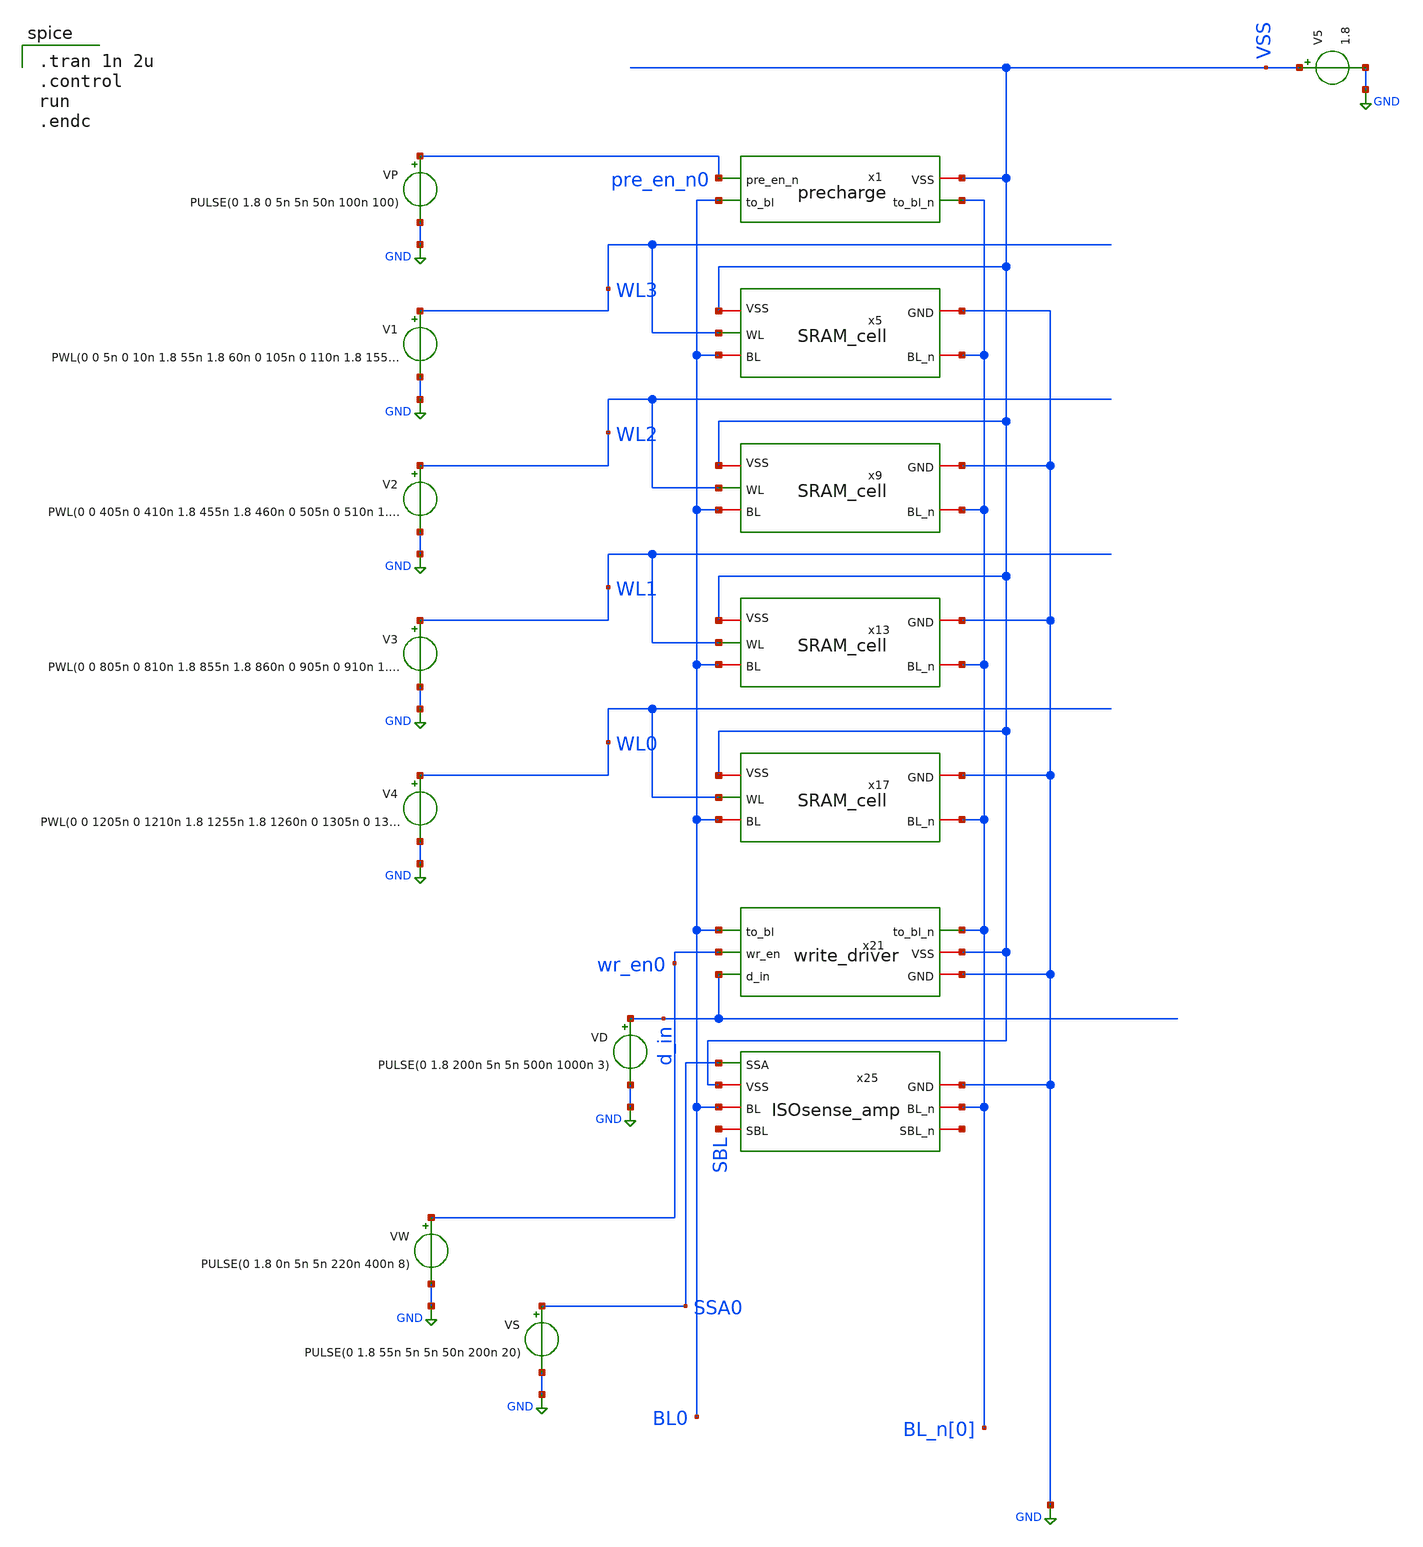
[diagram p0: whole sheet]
** sch_path: 4x1_SRAM.sch
**.subckt 4x1_SRAM
x1 VSS BL_n[0] BL0 pre_en_n0 precharge
x5 WL3 VSS BL_n[0] BL0 GND SRAM_cell
x9 WL2 VSS BL_n[0] BL0 GND SRAM_cell
x13 WL1 VSS BL_n[0] BL0 GND SRAM_cell
x17 WL0 VSS BL_n[0] BL0 GND SRAM_cell
x21 BL_n[0] BL0 wr_en0 VSS d_in GND write_driver
x25 SSA0 BL0 BL_n[0] VSS SBL net1 GND ISOsense_amp
VP pre_en_n0 GND PULSE(0 1.8 0 5n 5n 50n 100n 100)
V5 VSS GND 1.8
VW wr_en0 GND PULSE(0 1.8 0n 5n 5n 220n 400n 8)
VS SSA0 GND PULSE(0 1.8 55n 5n 5n 50n 200n 20)
V1 WL3 GND PWL(0 0 5n 0 10n 1.8 55n 1.8 60n 0 105n 0 110n 1.8 155n 1.8 160n 0 205n 0 210n 1.8 255n
+ 1.8 260n 0 305n 0 310n 1.8 355n 1.8 360n 0 1605n 0 1610n 1.8 1655n 1.8 1660n 0 2000n 0)
V2 WL2 GND PWL(0 0 405n 0 410n 1.8 455n 1.8 460n 0 505n 0 510n 1.8 555n 1.8 560n 0 605n 0 610n 1.8
+ 655n 1.8 660n 0 705n 0 710n 1.8 755n 1.8 760n 0 1705n 0 1710n 1.8 1755n 1.8 1760n 0 2000n 0)
V3 WL1 GND PWL(0 0 805n 0 810n 1.8 855n 1.8 860n 0 905n 0 910n 1.8 955n 1.8 960n 0 1005n 0 1010n 1.8
+ 1055n 1.8 1060n 0 1105n 0 1110n 1.8 1155n 1.8 1160n 0 1805n 0 1810n 1.8 1855n 1.8 1860n 0 2000n 0)
V4 WL0 GND PWL(0 0 1205n 0 1210n 1.8 1255n 1.8 1260n 0 1305n 0 1310n 1.8 1355n 1.8 1360n 0 1405n 0
+ 1410n 1.8 1455n 1.8 1460n 0 1505n 0 1510n 1.8 1555n 1.8 1560n 0 1905n 0 1910n 1.8 1955n 1.8 1960n 0 2000n
+ 0)
VD d_in GND PULSE(0 1.8 200n 5n 5n 500n 1000n 3)
**** begin user architecture code
 .lib $::SKYWATER_MODELS/sky130.lib.spice tt

.tran 1n 2u
.control
run
.endc

**** end user architecture code
**.ends

* expanding   symbol:  EE431_FINALPROJECT/proj_SRAM/precharge.sym # of pins=4
** sym_path: precharge.sym
** sch_path: precharge.sch
.subckt precharge VSS to_bl_n to_bl pre_en_n
*.ipin pre_en_n
*.opin to_bl
*.opin to_bl_n
*.iopin VSS
XM1 to_bl_n pre_en_n VSS VSS sky130_fd_pr__pfet_01v8 L=0.25 W=0.5 nf=1 ad='int((nf+1)/2) * W/nf * 0.29'
+ as='int((nf+2)/2) * W/nf * 0.29' pd='2*int((nf+1)/2) * (W/nf + 0.29)' ps='2*int((nf+2)/2) * (W/nf + 0.29)'
+ nrd='0.29 / W' nrs='0.29 / W' sa=0 sb=0 sd=0 mult=1 m=1
XM2 to_bl pre_en_n VSS VSS sky130_fd_pr__pfet_01v8 L=0.25 W=0.5 nf=1 ad='int((nf+1)/2) * W/nf * 0.29'
+ as='int((nf+2)/2) * W/nf * 0.29' pd='2*int((nf+1)/2) * (W/nf + 0.29)' ps='2*int((nf+2)/2) * (W/nf + 0.29)'
+ nrd='0.29 / W' nrs='0.29 / W' sa=0 sb=0 sd=0 mult=1 m=1
.ends


* expanding   symbol:  EE431_FINALPROJECT/proj_SRAM/SRAM_cell.sym # of pins=5
** sym_path: SRAM_cell.sym
** sch_path: SRAM_cell.sch
.subckt SRAM_cell WL VSS BL_n BL GND
*.ipin WL
*.iopin BL
*.iopin BL_n
*.iopin VSS
*.iopin GND
XM1 Q_n Q GND GND sky130_fd_pr__nfet_01v8 L=0.25 W=1.25 nf=1 ad='int((nf+1)/2) * W/nf * 0.29' as='int((nf+2)/2) * W/nf * 0.29'
+ pd='2*int((nf+1)/2) * (W/nf + 0.29)' ps='2*int((nf+2)/2) * (W/nf + 0.29)' nrd='0.29 / W' nrs='0.29 / W'
+ sa=0 sb=0 sd=0 mult=1 m=1
XM2 Q_n Q VSS VSS sky130_fd_pr__pfet_01v8 L=0.25 W=0.5 nf=1 ad='int((nf+1)/2) * W/nf * 0.29' as='int((nf+2)/2) * W/nf * 0.29'
+ pd='2*int((nf+1)/2) * (W/nf + 0.29)' ps='2*int((nf+2)/2) * (W/nf + 0.29)' nrd='0.29 / W' nrs='0.29 / W'
+ sa=0 sb=0 sd=0 mult=1 m=1
XM3 Q Q_n GND GND sky130_fd_pr__nfet_01v8 L=0.25 W=1.25 nf=1 ad='int((nf+1)/2) * W/nf * 0.29' as='int((nf+2)/2) * W/nf * 0.29'
+ pd='2*int((nf+1)/2) * (W/nf + 0.29)' ps='2*int((nf+2)/2) * (W/nf + 0.29)' nrd='0.29 / W' nrs='0.29 / W'
+ sa=0 sb=0 sd=0 mult=1 m=1
XM4 Q Q_n VSS VSS sky130_fd_pr__pfet_01v8 L=0.25 W=0.5 nf=1 ad='int((nf+1)/2) * W/nf * 0.29' as='int((nf+2)/2) * W/nf * 0.29'
+ pd='2*int((nf+1)/2) * (W/nf + 0.29)' ps='2*int((nf+2)/2) * (W/nf + 0.29)' nrd='0.29 / W' nrs='0.29 / W'
+ sa=0 sb=0 sd=0 mult=1 m=1
XM5 Q WL BL GND sky130_fd_pr__nfet_01v8 L=0.25 W=0.75 nf=1 ad='int((nf+1)/2) * W/nf * 0.29' as='int((nf+2)/2) * W/nf * 0.29'
+ pd='2*int((nf+1)/2) * (W/nf + 0.29)' ps='2*int((nf+2)/2) * (W/nf + 0.29)' nrd='0.29 / W' nrs='0.29 / W'
+ sa=0 sb=0 sd=0 mult=1 m=1
XM6 Q_n WL BL_n GND sky130_fd_pr__nfet_01v8 L=0.25 W=0.75 nf=1 ad='int((nf+1)/2) * W/nf * 0.29' as='int((nf+2)/2) * W/nf * 0.29'
+ pd='2*int((nf+1)/2) * (W/nf + 0.29)' ps='2*int((nf+2)/2) * (W/nf + 0.29)' nrd='0.29 / W' nrs='0.29 / W'
+ sa=0 sb=0 sd=0 mult=1 m=1
.ends


* expanding   symbol:  EE431_FINALPROJECT/proj_SRAM/write_driver.sym # of pins=6
** sym_path: write_driver.sym
** sch_path: write_driver.sch
.subckt write_driver to_bl_n to_bl wr_en VSS d_in GND
*.ipin d_in
*.ipin wr_en
*.opin to_bl
*.opin to_bl_n
*.iopin VSS
*.iopin GND
XM1 to_bl wr_en d_in GND sky130_fd_pr__nfet_01v8 L=0.25 W=1 nf=1 ad='int((nf+1)/2) * W/nf * 0.29' as='int((nf+2)/2) * W/nf * 0.29'
+ pd='2*int((nf+1)/2) * (W/nf + 0.29)' ps='2*int((nf+2)/2) * (W/nf + 0.29)' nrd='0.29 / W' nrs='0.29 / W'
+ sa=0 sb=0 sd=0 mult=1 m=1
XM2 to_bl_n wr_en d_n GND sky130_fd_pr__nfet_01v8 L=0.25 W=1 nf=1 ad='int((nf+1)/2) * W/nf * 0.29' as='int((nf+2)/2) * W/nf * 0.29'
+ pd='2*int((nf+1)/2) * (W/nf + 0.29)' ps='2*int((nf+2)/2) * (W/nf + 0.29)' nrd='0.29 / W' nrs='0.29 / W'
+ sa=0 sb=0 sd=0 mult=1 m=1
XM3 d_n d_in VSS VSS sky130_fd_pr__pfet_01v8 L=0.25 W=1 nf=1 ad='int((nf+1)/2) * W/nf * 0.29' as='int((nf+2)/2) * W/nf * 0.29'
+ pd='2*int((nf+1)/2) * (W/nf + 0.29)' ps='2*int((nf+2)/2) * (W/nf + 0.29)' nrd='0.29 / W' nrs='0.29 / W'
+ sa=0 sb=0 sd=0 mult=1 m=1
XM4 d_n d_in GND GND sky130_fd_pr__nfet_01v8 L=0.25 W=0.5 nf=1 ad='int((nf+1)/2) * W/nf * 0.29' as='int((nf+2)/2) * W/nf * 0.29'
+ pd='2*int((nf+1)/2) * (W/nf + 0.29)' ps='2*int((nf+2)/2) * (W/nf + 0.29)' nrd='0.29 / W' nrs='0.29 / W'
+ sa=0 sb=0 sd=0 mult=1 m=1
.ends


* expanding   symbol:  EE431_FINALPROJECT/proj_SRAM/ISOsense_amp.sym # of pins=7
** sym_path: ISOsense_amp.sym
** sch_path: ISOsense_amp.sch
.subckt ISOsense_amp SSA BL BL_n VSS SBL SBL_n GND
*.iopin VSS
*.iopin BL_n
*.iopin BL
*.iopin GND
*.ipin SSA
*.iopin SBL
*.iopin SBL_n
XM1 SBL_n SBL net1 GND sky130_fd_pr__nfet_01v8 L=0.25 W=1 nf=1 ad='int((nf+1)/2) * W/nf * 0.29' as='int((nf+2)/2) * W/nf * 0.29'
+ pd='2*int((nf+1)/2) * (W/nf + 0.29)' ps='2*int((nf+2)/2) * (W/nf + 0.29)' nrd='0.29 / W' nrs='0.29 / W'
+ sa=0 sb=0 sd=0 mult=1 m=1
XM2 SBL SBL_n net1 GND sky130_fd_pr__nfet_01v8 L=0.25 W=1 nf=1 ad='int((nf+1)/2) * W/nf * 0.29' as='int((nf+2)/2) * W/nf * 0.29'
+ pd='2*int((nf+1)/2) * (W/nf + 0.29)' ps='2*int((nf+2)/2) * (W/nf + 0.29)' nrd='0.29 / W' nrs='0.29 / W'
+ sa=0 sb=0 sd=0 mult=1 m=1
XM3 SBL_n SBL VSS VSS sky130_fd_pr__pfet_01v8 L=0.25 W=2 nf=1 ad='int((nf+1)/2) * W/nf * 0.29' as='int((nf+2)/2) * W/nf * 0.29'
+ pd='2*int((nf+1)/2) * (W/nf + 0.29)' ps='2*int((nf+2)/2) * (W/nf + 0.29)' nrd='0.29 / W' nrs='0.29 / W'
+ sa=0 sb=0 sd=0 mult=1 m=1
XM4 SBL SBL_n VSS VSS sky130_fd_pr__pfet_01v8 L=0.25 W=2 nf=1 ad='int((nf+1)/2) * W/nf * 0.29' as='int((nf+2)/2) * W/nf * 0.29'
+ pd='2*int((nf+1)/2) * (W/nf + 0.29)' ps='2*int((nf+2)/2) * (W/nf + 0.29)' nrd='0.29 / W' nrs='0.29 / W'
+ sa=0 sb=0 sd=0 mult=1 m=1
XM5 net1 SSA GND GND sky130_fd_pr__nfet_01v8 L=0.25 W=2 nf=1 ad='int((nf+1)/2) * W/nf * 0.29' as='int((nf+2)/2) * W/nf * 0.29'
+ pd='2*int((nf+1)/2) * (W/nf + 0.29)' ps='2*int((nf+2)/2) * (W/nf + 0.29)' nrd='0.29 / W' nrs='0.29 / W'
+ sa=0 sb=0 sd=0 mult=1 m=1
XM6 SBL SSA BL VSS sky130_fd_pr__pfet_01v8 L=0.25 W=0.5 nf=1 ad='int((nf+1)/2) * W/nf * 0.29' as='int((nf+2)/2) * W/nf * 0.29'
+ pd='2*int((nf+1)/2) * (W/nf + 0.29)' ps='2*int((nf+2)/2) * (W/nf + 0.29)' nrd='0.29 / W' nrs='0.29 / W'
+ sa=0 sb=0 sd=0 mult=1 m=1
XM7 SBL_n SSA BL_n VSS sky130_fd_pr__pfet_01v8 L=0.25 W=0.5 nf=1 ad='int((nf+1)/2) * W/nf * 0.29' as='int((nf+2)/2) * W/nf * 0.29'
+ pd='2*int((nf+1)/2) * (W/nf + 0.29)' ps='2*int((nf+2)/2) * (W/nf + 0.29)' nrd='0.29 / W' nrs='0.29 / W'
+ sa=0 sb=0 sd=0 mult=1 m=1
.ends

.GLOBAL GND
.end
